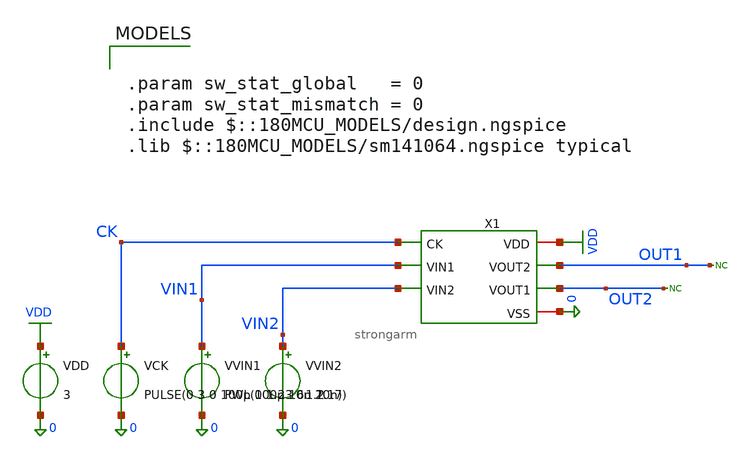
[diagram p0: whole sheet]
** sch_path: comparator/schematic/strongarm_mc_tb.sch
**.subckt strongarm_mc_tb
X1 VDD CK OUT1 OUT2 VIN1 VIN2 0 strongarm
VVIN2 VIN2 0 1.2
VVIN1 VIN1 0 PWL(0 1.23 6u 1.17)
VDD VDD 0 3
VCK CK 0 PULSE(0 3 0 100p 100p 10n 20n)
* noconn OUT2
* noconn OUT1
**** begin user architecture code

.param sw_stat_global   = 0
.param sw_stat_mismatch = 0
.include $::180MCU_MODELS/design.ngspice
.lib $::180MCU_MODELS/sm141064.ngspice typical



.control
* ============================================================
* StrongArm comparator — input-referred offset Monte Carlo
* offset = midpoint of UP-sweep and DOWN-sweep trip points.
* RULE: never put '>' inside a 'let' — ngspice reads it as a file
* redirect. Comparisons are only safe inside 'if'.
* MODELS block must have: sw_stat_mismatch=0, sw_stat_global=0
* ============================================================

let mc_runs = 100
let svt     = 24.8e-3
let run     = 0
let offset_results = vector(mc_runs)
let ngood = 0
let sumx  = 0
let sumx2 = 0
set homeplot = $curplot

dowhile run < mc_runs
  echo ---- run $&run ----
  unset s_up
  unset s_dn

  * fresh mismatch draw, applied to both sweeps
  alter @m.x1.xm10.m0[delvto] = svt * sgauss(0)
  alter @m.x1.xm8.m0[delvto]  = svt * sgauss(0)

  * -------- UP sweep: VIN1 1.05 -> 1.35 --------
  alter @vvin1[pwl] = [ 0 1.05 6e-6 1.35 ]
  tran 10p 6u
  let t_up = -1
  meas tran t_up when v(out1)=1.5 fall=LAST
  if t_up > 0
    meas tran vin_up find v(vin1) at=t_up
    set s_up = $&vin_up
  end
  destroy $curplot

  * -------- DOWN sweep: VIN1 1.35 -> 1.05 --------
  alter @vvin1[pwl] = [ 0 1.35 6e-6 1.05 ]
  tran 10p 6u
  let t_dn = -1
  meas tran t_dn when v(out1)=1.5 fall=1
  if t_dn > 0
    meas tran vin_dn find v(vin1) at=t_dn
    set s_dn = $&vin_dn
  end
  destroy $curplot

  * -------- combine, back in the home plot --------
  setplot $homeplot
  if $?s_up * $?s_dn
    let cur = (($s_up - 1.2) + ($s_dn - 1.2)) / 2
    let offset_results[run] = cur
    let ngood = ngood + 1
    let sumx  = sumx  + cur
    let sumx2 = sumx2 + cur*cur
    echo   up=$s_up dn=$s_dn offset=$&cur
  else
    let offset_results[run] = -999
    echo   WARN: miss on run $&run
  end

  let run = run + 1
end

* ================= stats (valid runs only) =================
setplot $homeplot
let mu  = sumx / ngood
let sig = sqrt( sumx2/ngood - mu*mu )
echo ======================================================
echo MC done: N=$&mc_runs  good=$&ngood
echo   mean offset = $&mu V
echo   sigma       = $&sig V
echo ======================================================

unset wr_singlescale
write  /foss/designs/comparator/comp_mc_offsets.raw offset_results
wrdata /foss/designs/comparator/comp_mc_offsets.txt offset_results
echo MC N=$&mc_runs good=$&ngood mean=$&mu sigma=$&sig > /foss/designs/comparator/comp_mc_report.txt
print offset_results >> /foss/designs/comparator/comp_mc_report.txt
.endc


**** end user architecture code
**.ends

* expanding   symbol:  comparator/schematic/strongarm.sym # of pins=7
** sym_path: comparator/schematic/strongarm.sym
** sch_path: comparator/schematic/strongarm.sch
.subckt strongarm VDD CK VOUT2 VOUT1 VIN1 VIN2 VSS
*.opin VOUT1
*.opin VOUT2
*.ipin VIN1
*.ipin VIN2
*.ipin CK
*.iopin VDD
*.iopin VSS
XM1 VOUT2 VOUT1 net1 net1 nfet_03v3 L=0.28u W=0.22u nf=1 ad='int((nf+1)/2) * W/nf * 0.18u' as='int((nf+2)/2) * W/nf * 0.18u'
+ pd='2*int((nf+1)/2) * (W/nf + 0.18u)' ps='2*int((nf+2)/2) * (W/nf + 0.18u)' nrd='0.18u / W' nrs='0.18u / W'
+ sa=0 sb=0 sd=0 m=1
XM2 VOUT1 VOUT2 VDD VDD pfet_03v3 L=0.28u W=0.22u nf=1 ad='int((nf+1)/2) * W/nf * 0.18u' as='int((nf+2)/2) * W/nf * 0.18u'
+ pd='2*int((nf+1)/2) * (W/nf + 0.18u)' ps='2*int((nf+2)/2) * (W/nf + 0.18u)' nrd='0.18u / W' nrs='0.18u / W'
+ sa=0 sb=0 sd=0 m=1
XM3 VOUT1 CK VDD VDD pfet_03v3 L=0.28u W=0.22u nf=1 ad='int((nf+1)/2) * W/nf * 0.18u' as='int((nf+2)/2) * W/nf * 0.18u'
+ pd='2*int((nf+1)/2) * (W/nf + 0.18u)' ps='2*int((nf+2)/2) * (W/nf + 0.18u)' nrd='0.18u / W' nrs='0.18u / W'
+ sa=0 sb=0 sd=0 m=1
XM4 net3 CK VDD VDD pfet_03v3 L=0.28u W=0.22u nf=1 ad='int((nf+1)/2) * W/nf * 0.18u' as='int((nf+2)/2) * W/nf * 0.18u'
+ pd='2*int((nf+1)/2) * (W/nf + 0.18u)' ps='2*int((nf+2)/2) * (W/nf + 0.18u)' nrd='0.18u / W' nrs='0.18u / W'
+ sa=0 sb=0 sd=0 m=1
XM5 net1 CK VDD VDD pfet_03v3 L=0.28u W=0.22u nf=1 ad='int((nf+1)/2) * W/nf * 0.18u' as='int((nf+2)/2) * W/nf * 0.18u'
+ pd='2*int((nf+1)/2) * (W/nf + 0.18u)' ps='2*int((nf+2)/2) * (W/nf + 0.18u)' nrd='0.18u / W' nrs='0.18u / W'
+ sa=0 sb=0 sd=0 m=1
XM6 VOUT2 CK VDD VDD pfet_03v3 L=0.28u W=0.22u nf=1 ad='int((nf+1)/2) * W/nf * 0.18u' as='int((nf+2)/2) * W/nf * 0.18u'
+ pd='2*int((nf+1)/2) * (W/nf + 0.18u)' ps='2*int((nf+2)/2) * (W/nf + 0.18u)' nrd='0.18u / W' nrs='0.18u / W'
+ sa=0 sb=0 sd=0 m=1
XM7 VOUT2 VOUT1 VDD VDD pfet_03v3 L=0.28u W=0.22u nf=1 ad='int((nf+1)/2) * W/nf * 0.18u' as='int((nf+2)/2) * W/nf * 0.18u'
+ pd='2*int((nf+1)/2) * (W/nf + 0.18u)' ps='2*int((nf+2)/2) * (W/nf + 0.18u)' nrd='0.18u / W' nrs='0.18u / W'
+ sa=0 sb=0 sd=0 m=1
XM8 net1 VIN2 net2 net2 nfet_03v3 L=0.28u W=0.22u nf=1 ad='int((nf+1)/2) * W/nf * 0.18u' as='int((nf+2)/2) * W/nf * 0.18u'
+ pd='2*int((nf+1)/2) * (W/nf + 0.18u)' ps='2*int((nf+2)/2) * (W/nf + 0.18u)' nrd='0.18u / W' nrs='0.18u / W'
+ sa=0 sb=0 sd=0 m=1
XM9 VOUT1 VOUT2 net3 net3 nfet_03v3 L=0.28u W=0.22u nf=1 ad='int((nf+1)/2) * W/nf * 0.18u' as='int((nf+2)/2) * W/nf * 0.18u'
+ pd='2*int((nf+1)/2) * (W/nf + 0.18u)' ps='2*int((nf+2)/2) * (W/nf + 0.18u)' nrd='0.18u / W' nrs='0.18u / W'
+ sa=0 sb=0 sd=0 m=1
XM10 net3 VIN1 net2 net2 nfet_03v3 L=0.28u W=0.22u nf=1 ad='int((nf+1)/2) * W/nf * 0.18u' as='int((nf+2)/2) * W/nf * 0.18u'
+ pd='2*int((nf+1)/2) * (W/nf + 0.18u)' ps='2*int((nf+2)/2) * (W/nf + 0.18u)' nrd='0.18u / W' nrs='0.18u / W'
+ sa=0 sb=0 sd=0 m=1
XM11 net2 CK VSS net2 nfet_03v3 L=0.28u W=0.22u nf=1 ad='int((nf+1)/2) * W/nf * 0.18u' as='int((nf+2)/2) * W/nf * 0.18u'
+ pd='2*int((nf+1)/2) * (W/nf + 0.18u)' ps='2*int((nf+2)/2) * (W/nf + 0.18u)' nrd='0.18u / W' nrs='0.18u / W'
+ sa=0 sb=0 sd=0 m=1
.ends

.GLOBAL VDD
.end
